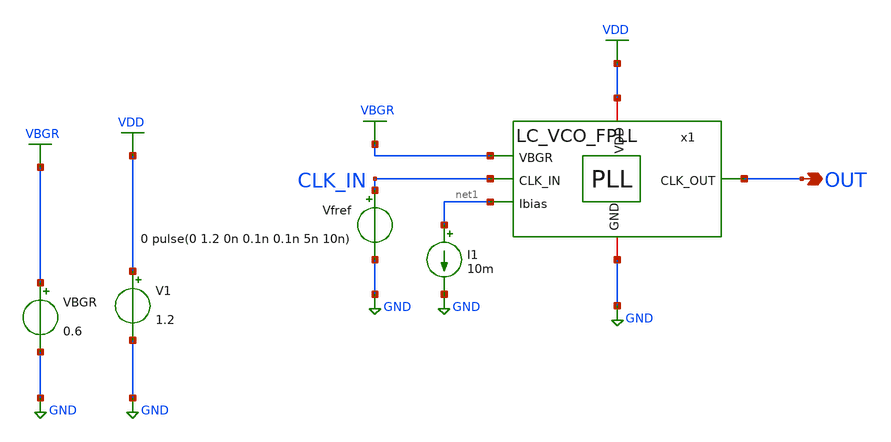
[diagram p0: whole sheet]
** sch_path: schematic/top-pll/LC_VCO_PLL_op_tb.sch
**.subckt LC_VCO_PLL_op_tb OUT
*.opin OUT
Vfref CLK_IN GND 0 pulse(0 1.2 0n 0.1n 0.1n 5n 10n)
I1 net1 GND 10m
x1 VDD CLK_IN OUT VBGR net1 GND LC_VCO_FPLL
V1 VDD GND 1.2
VBGR VBGR GND 0.6
**** begin user architecture code



*****************************************************
* PLL + DSM Frequency Divider Testbench
*****************************************************

.option temp = 27
.param VDD = 1.2

* ==============================
* Include Models
* ==============================

* Inductor / analog models
.include ./IHP_4nH_Inductor.spice

.control
save all
op
set filetype=ascii

* Print supply current
print i(V1)

* Print power (correct way)
let power = i(V1)*v(VDD)
print power

write op_out.raw
print all > op_out.txt
.endc

* to generate following file copy stimuli.test
* to the simulation directory and run simulation -> Utile Stimuli Editor (GUI),
* and press 'Translate'
.include stimuli_test.cir






.lib cornerMOSlv.lib mos_tt
.lib cornerMOShv.lib mos_tt
.lib cornerHBT.lib hbt_typ
.lib cornerRES.lib res_typ
.lib cornerCAP.lib cap_typ_stat
.include /foss/pdks/ihp-sg13g2/libs.ref/sg13g2_stdcell/spice/sg13g2_stdcell.spice
.global VDD GND


.param CP_N_L = 1u
.param CP_N_W = 3u
.param CP_P_M = 1
.param CP_P_L = 1u
.param CP_P_W = 10u
.param CP_N_M = 1



**** end user architecture code
**.ends
.GLOBAL GND
.GLOBAL VDD
.GLOBAL VBGR
.end
